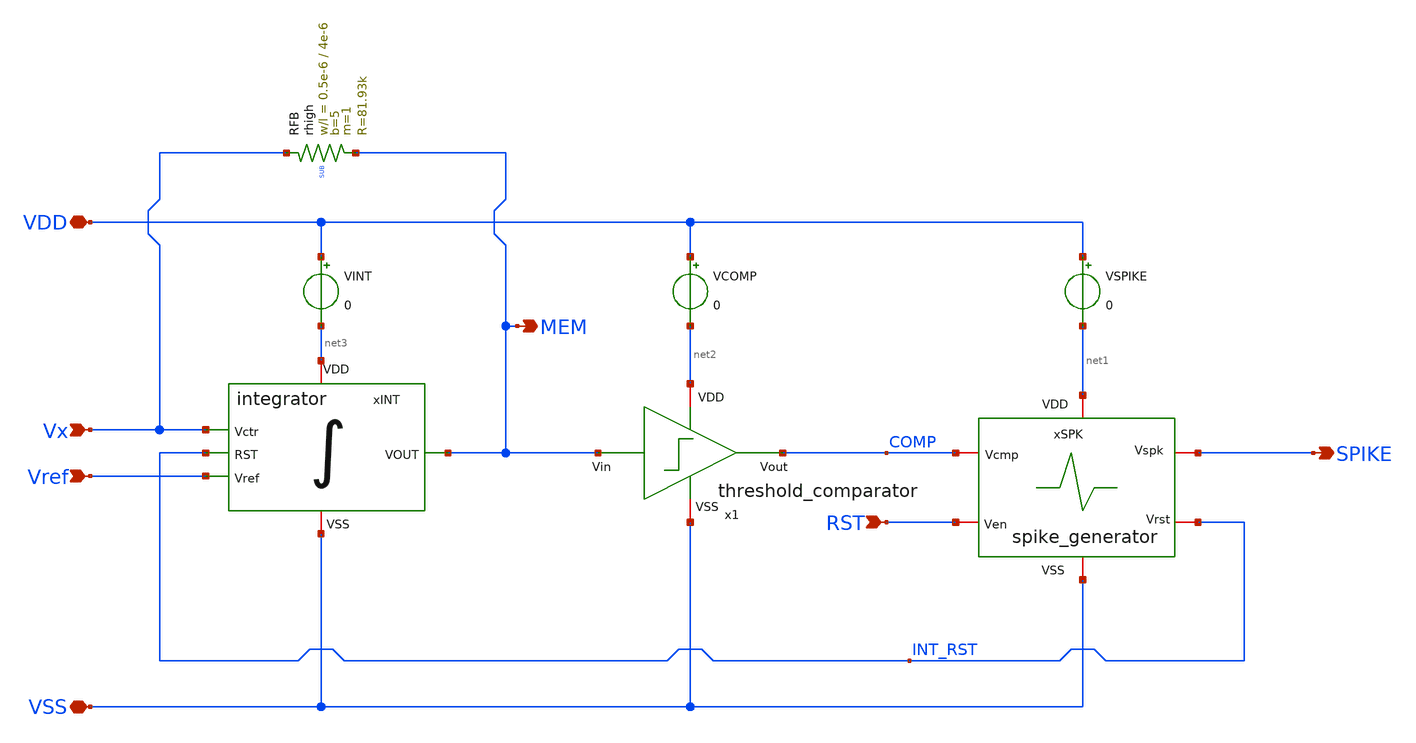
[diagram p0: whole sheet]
** sch_path: work/LIF_Neuron/xschem/LIF_neuron.sch
**.subckt LIF_neuron VDD VSS MEM Vx Vref SPIKE RST
*.iopin VDD
*.iopin VSS
*.opin MEM
*.ipin Vx
*.ipin Vref
*.opin SPIKE
*.ipin RST
xINT Vref VSS net3 INT_RST Vx MEM integrator
xSPK net1 COMP SPIKE INT_RST RST VSS spike_generator
VINT VDD net3 0
VCOMP VDD net2 0
VSPIKE VDD net1 0
XRFB Vx MEM SUB rhigh w=0.5e-6 l=4e-6 m=1 b=5 mm_ok=1
x1 net2 MEM COMP VSS threshold_comparator
**.ends
.end
